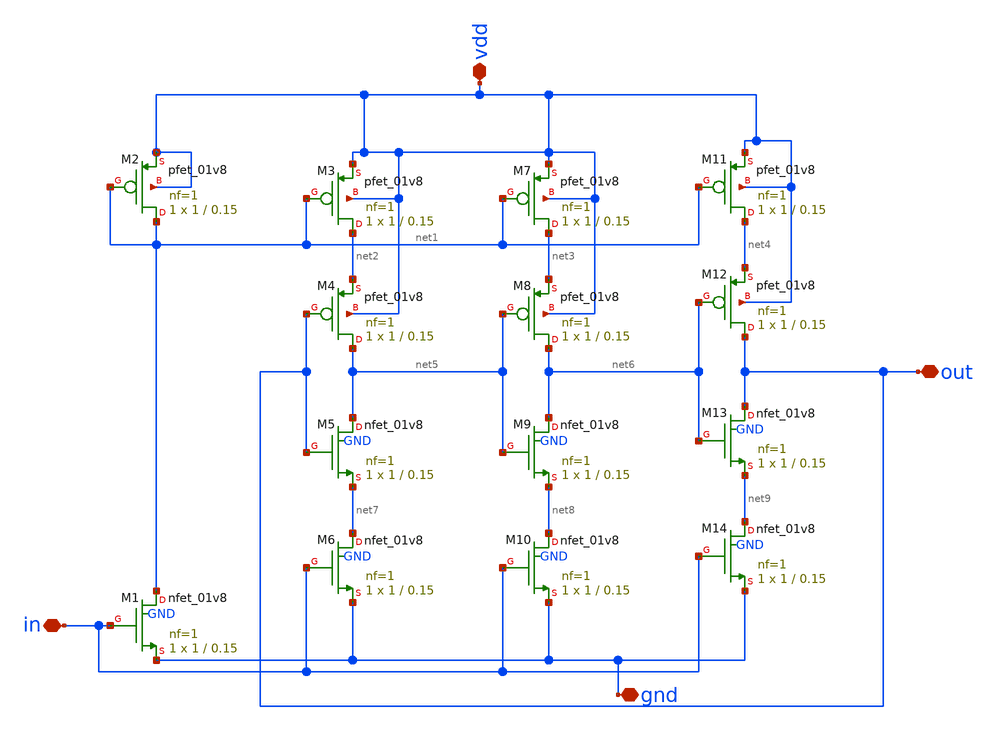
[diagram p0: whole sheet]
** sch_path: vco_sky130.sch
**.subckt vco_sky130 vdd in gnd out
*.iopin vdd
*.iopin in
*.iopin gnd
*.iopin out
XM2 net1 net1 vdd vdd sky130_fd_pr__pfet_01v8 L=0.15 W=1 nf=1 ad='int((1 + 1)/2) * 1 / 1 * 0.29' as='int((1 + 2)/2) * 1 / 1 * 0.29'
+ pd='2*int((1 + 1)/2) * (1 / 1 + 0.29)' ps='2*int((1 + 2)/2) * (1 / 1 + 0.29)' nrd='0.29 / 1 ' nrs='0.29 / 1 '
+ sa=0 sb=0 sd=0 mult=1 m=1
XM1 net1 in gnd GND sky130_fd_pr__nfet_01v8 L=0.15 W=1 nf=1 ad='int((1 + 1)/2) * 1 / 1 * 0.29' as='int((1 + 2)/2) * 1 / 1 * 0.29'
+ pd='2*int((1 + 1)/2) * (1 / 1 + 0.29)' ps='2*int((1 + 2)/2) * (1 / 1 + 0.29)' nrd='0.29 / 1 ' nrs='0.29 / 1 '
+ sa=0 sb=0 sd=0 mult=1 m=1
XM3 net2 net1 vdd vdd sky130_fd_pr__pfet_01v8 L=0.15 W=1 nf=1 ad='int((1 + 1)/2) * 1 / 1 * 0.29' as='int((1 + 2)/2) * 1 / 1 * 0.29'
+ pd='2*int((1 + 1)/2) * (1 / 1 + 0.29)' ps='2*int((1 + 2)/2) * (1 / 1 + 0.29)' nrd='0.29 / 1 ' nrs='0.29 / 1 '
+ sa=0 sb=0 sd=0 mult=1 m=1
XM4 net5 out net2 vdd sky130_fd_pr__pfet_01v8 L=0.15 W=1 nf=1 ad='int((1 + 1)/2) * 1 / 1 * 0.29' as='int((1 + 2)/2) * 1 / 1 * 0.29'
+ pd='2*int((1 + 1)/2) * (1 / 1 + 0.29)' ps='2*int((1 + 2)/2) * (1 / 1 + 0.29)' nrd='0.29 / 1 ' nrs='0.29 / 1 '
+ sa=0 sb=0 sd=0 mult=1 m=1
XM5 net5 out net7 GND sky130_fd_pr__nfet_01v8 L=0.15 W=1 nf=1 ad='int((1 + 1)/2) * 1 / 1 * 0.29' as='int((1 + 2)/2) * 1 / 1 * 0.29'
+ pd='2*int((1 + 1)/2) * (1 / 1 + 0.29)' ps='2*int((1 + 2)/2) * (1 / 1 + 0.29)' nrd='0.29 / 1 ' nrs='0.29 / 1 '
+ sa=0 sb=0 sd=0 mult=1 m=1
XM6 net7 in gnd GND sky130_fd_pr__nfet_01v8 L=0.15 W=1 nf=1 ad='int((1 + 1)/2) * 1 / 1 * 0.29' as='int((1 + 2)/2) * 1 / 1 * 0.29'
+ pd='2*int((1 + 1)/2) * (1 / 1 + 0.29)' ps='2*int((1 + 2)/2) * (1 / 1 + 0.29)' nrd='0.29 / 1 ' nrs='0.29 / 1 '
+ sa=0 sb=0 sd=0 mult=1 m=1
XM7 net3 net1 vdd vdd sky130_fd_pr__pfet_01v8 L=0.15 W=1 nf=1 ad='int((1 + 1)/2) * 1 / 1 * 0.29' as='int((1 + 2)/2) * 1 / 1 * 0.29'
+ pd='2*int((1 + 1)/2) * (1 / 1 + 0.29)' ps='2*int((1 + 2)/2) * (1 / 1 + 0.29)' nrd='0.29 / 1 ' nrs='0.29 / 1 '
+ sa=0 sb=0 sd=0 mult=1 m=1
XM8 net6 net5 net3 vdd sky130_fd_pr__pfet_01v8 L=0.15 W=1 nf=1 ad='int((1 + 1)/2) * 1 / 1 * 0.29' as='int((1 + 2)/2) * 1 / 1 * 0.29'
+ pd='2*int((1 + 1)/2) * (1 / 1 + 0.29)' ps='2*int((1 + 2)/2) * (1 / 1 + 0.29)' nrd='0.29 / 1 ' nrs='0.29 / 1 '
+ sa=0 sb=0 sd=0 mult=1 m=1
XM9 net6 net5 net8 GND sky130_fd_pr__nfet_01v8 L=0.15 W=1 nf=1 ad='int((1 + 1)/2) * 1 / 1 * 0.29' as='int((1 + 2)/2) * 1 / 1 * 0.29'
+ pd='2*int((1 + 1)/2) * (1 / 1 + 0.29)' ps='2*int((1 + 2)/2) * (1 / 1 + 0.29)' nrd='0.29 / 1 ' nrs='0.29 / 1 '
+ sa=0 sb=0 sd=0 mult=1 m=1
XM10 net8 in gnd GND sky130_fd_pr__nfet_01v8 L=0.15 W=1 nf=1 ad='int((1 + 1)/2) * 1 / 1 * 0.29' as='int((1 + 2)/2) * 1 / 1 * 0.29'
+ pd='2*int((1 + 1)/2) * (1 / 1 + 0.29)' ps='2*int((1 + 2)/2) * (1 / 1 + 0.29)' nrd='0.29 / 1 ' nrs='0.29 / 1 '
+ sa=0 sb=0 sd=0 mult=1 m=1
XM11 net4 net1 vdd vdd sky130_fd_pr__pfet_01v8 L=0.15 W=1 nf=1 ad='int((1 + 1)/2) * 1 / 1 * 0.29' as='int((1 + 2)/2) * 1 / 1 * 0.29'
+ pd='2*int((1 + 1)/2) * (1 / 1 + 0.29)' ps='2*int((1 + 2)/2) * (1 / 1 + 0.29)' nrd='0.29 / 1 ' nrs='0.29 / 1 '
+ sa=0 sb=0 sd=0 mult=1 m=1
XM12 out net6 net4 vdd sky130_fd_pr__pfet_01v8 L=0.15 W=1 nf=1 ad='int((1 + 1)/2) * 1 / 1 * 0.29' as='int((1 + 2)/2) * 1 / 1 * 0.29'
+ pd='2*int((1 + 1)/2) * (1 / 1 + 0.29)' ps='2*int((1 + 2)/2) * (1 / 1 + 0.29)' nrd='0.29 / 1 ' nrs='0.29 / 1 '
+ sa=0 sb=0 sd=0 mult=1 m=1
XM13 out net6 net9 GND sky130_fd_pr__nfet_01v8 L=0.15 W=1 nf=1 ad='int((1 + 1)/2) * 1 / 1 * 0.29' as='int((1 + 2)/2) * 1 / 1 * 0.29'
+ pd='2*int((1 + 1)/2) * (1 / 1 + 0.29)' ps='2*int((1 + 2)/2) * (1 / 1 + 0.29)' nrd='0.29 / 1 ' nrs='0.29 / 1 '
+ sa=0 sb=0 sd=0 mult=1 m=1
XM14 net9 in gnd GND sky130_fd_pr__nfet_01v8 L=0.15 W=1 nf=1 ad='int((1 + 1)/2) * 1 / 1 * 0.29' as='int((1 + 2)/2) * 1 / 1 * 0.29'
+ pd='2*int((1 + 1)/2) * (1 / 1 + 0.29)' ps='2*int((1 + 2)/2) * (1 / 1 + 0.29)' nrd='0.29 / 1 ' nrs='0.29 / 1 '
+ sa=0 sb=0 sd=0 mult=1 m=1
**.ends
.end
